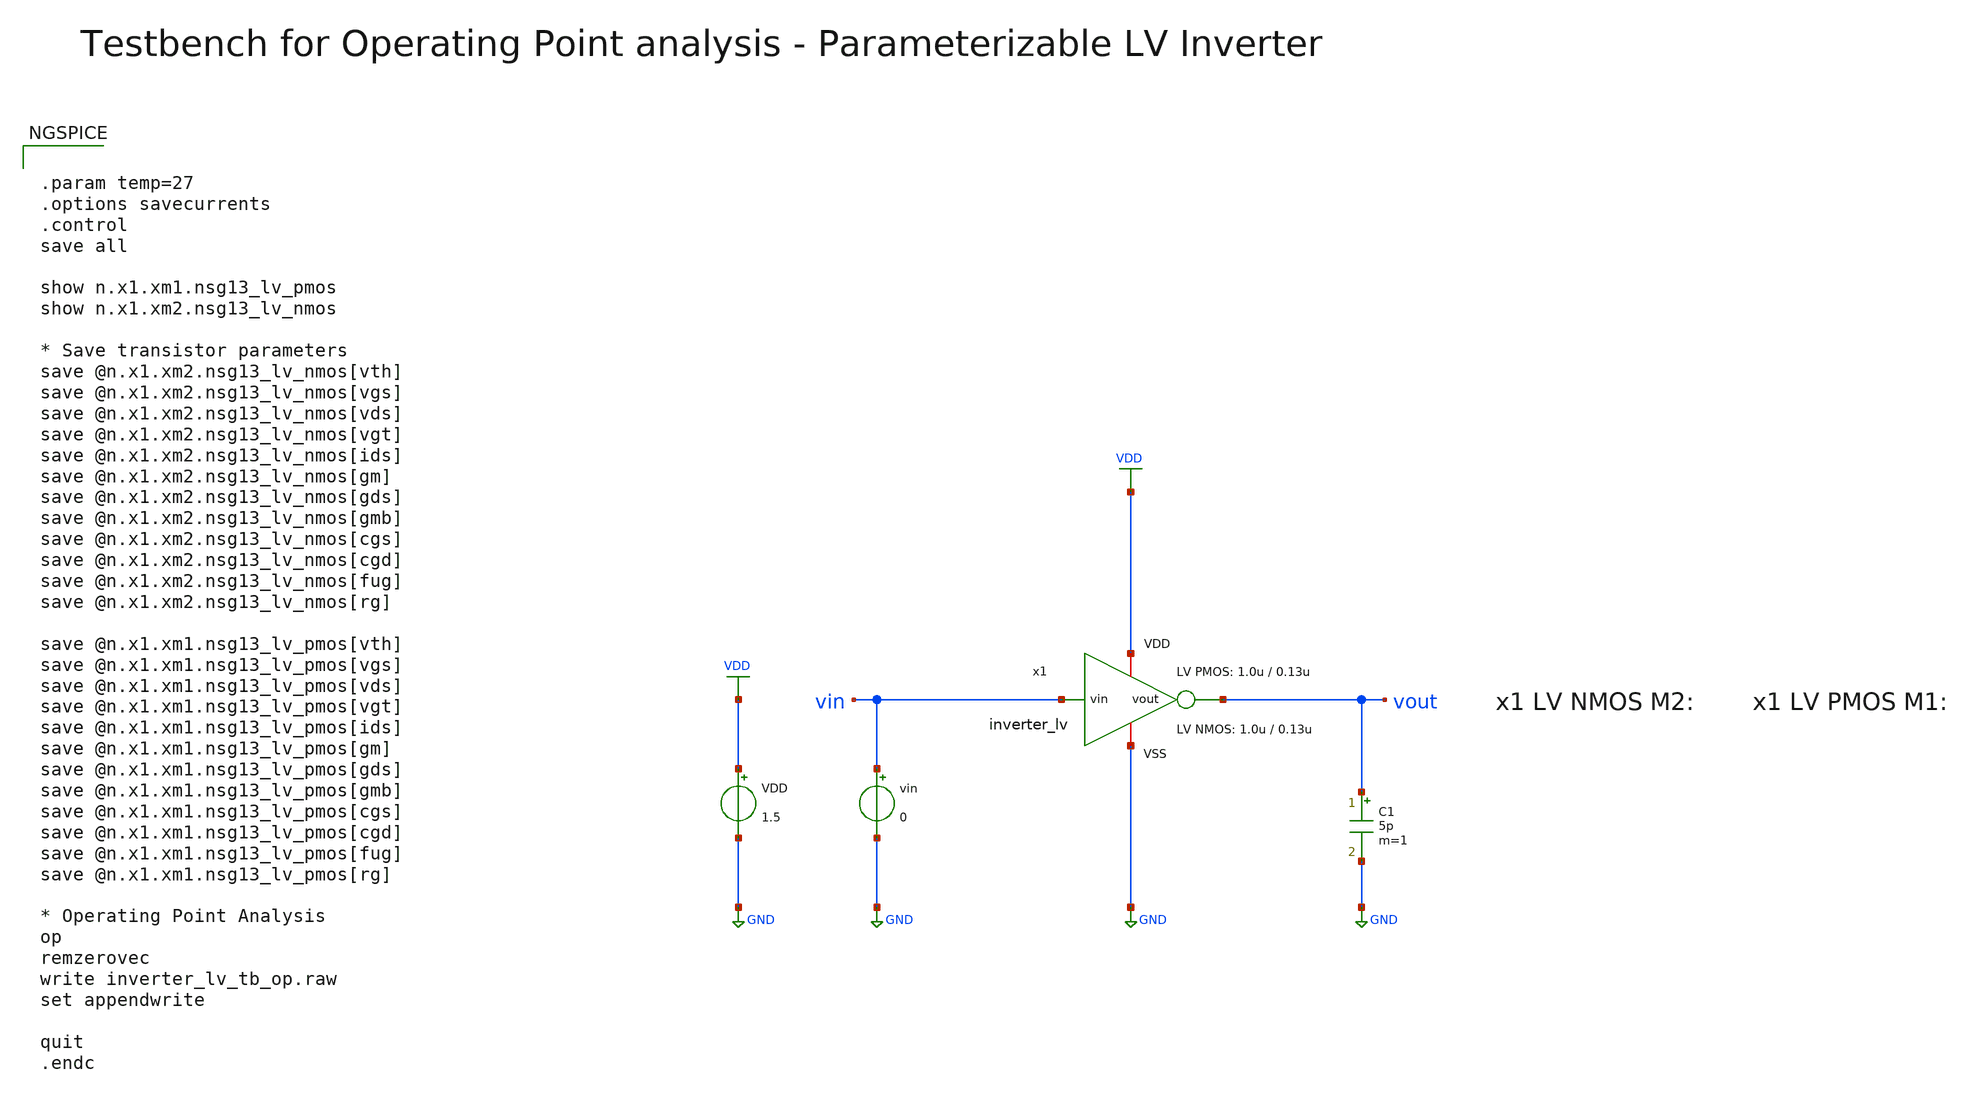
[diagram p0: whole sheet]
** sch_path: SG13G2_ATBS-ADC-main/xschem/inverter/testbenches/inverter_lv_tb_op.sch
**.subckt inverter_lv_tb_op
VDD VDD GND 1.5
C1 vout GND 5p m=1
vin vin GND 0
x1 VDD vin vout GND inverter_lv W_P=1.0u L_P=0.13u W_N=1.0u L_N=0.13u
**** begin user architecture code

.lib cornerMOSlv.lib mos_tt
.lib cornerRES.lib res_typ



.param temp=27
.options savecurrents
.control
save all

show n.x1.xm1.nsg13_lv_pmos
show n.x1.xm2.nsg13_lv_nmos

* Save transistor parameters
save @n.x1.xm2.nsg13_lv_nmos[vth]
save @n.x1.xm2.nsg13_lv_nmos[vgs]
save @n.x1.xm2.nsg13_lv_nmos[vds]
save @n.x1.xm2.nsg13_lv_nmos[vgt]
save @n.x1.xm2.nsg13_lv_nmos[ids]
save @n.x1.xm2.nsg13_lv_nmos[gm]
save @n.x1.xm2.nsg13_lv_nmos[gds]
save @n.x1.xm2.nsg13_lv_nmos[gmb]
save @n.x1.xm2.nsg13_lv_nmos[cgs]
save @n.x1.xm2.nsg13_lv_nmos[cgd]
save @n.x1.xm2.nsg13_lv_nmos[fug]
save @n.x1.xm2.nsg13_lv_nmos[rg]

save @n.x1.xm1.nsg13_lv_pmos[vth]
save @n.x1.xm1.nsg13_lv_pmos[vgs]
save @n.x1.xm1.nsg13_lv_pmos[vds]
save @n.x1.xm1.nsg13_lv_pmos[vgt]
save @n.x1.xm1.nsg13_lv_pmos[ids]
save @n.x1.xm1.nsg13_lv_pmos[gm]
save @n.x1.xm1.nsg13_lv_pmos[gds]
save @n.x1.xm1.nsg13_lv_pmos[gmb]
save @n.x1.xm1.nsg13_lv_pmos[cgs]
save @n.x1.xm1.nsg13_lv_pmos[cgd]
save @n.x1.xm1.nsg13_lv_pmos[fug]
save @n.x1.xm1.nsg13_lv_pmos[rg]

* Operating Point Analysis
op
remzerovec
write inverter_lv_tb_op.raw
set appendwrite

quit
.endc

**** end user architecture code
**.ends

* expanding   symbol:  inverter/inverter_lv.sym # of pins=4
** sym_path: SG13G2_ATBS-ADC-main/xschem/inverter/inverter_lv.sym
** sch_path: SG13G2_ATBS-ADC-main/xschem/inverter/inverter_lv.sch
.subckt inverter_lv VDD vin vout VSS  W_P=3.0u L_P=0.13u W_N=1.0u L_N=0.13u
*.ipin vin
*.iopin VDD
*.iopin VSS
*.opin vout
XM1 vout vin VDD VDD sg13_lv_pmos w=W_P l=L_P ng=1 m=1 mm_ok=1
XM2 vout vin VSS VSS sg13_lv_nmos w=W_N l=L_N ng=1 m=1 mm_ok=1
.ends

.GLOBAL GND
.GLOBAL VDD
.end
